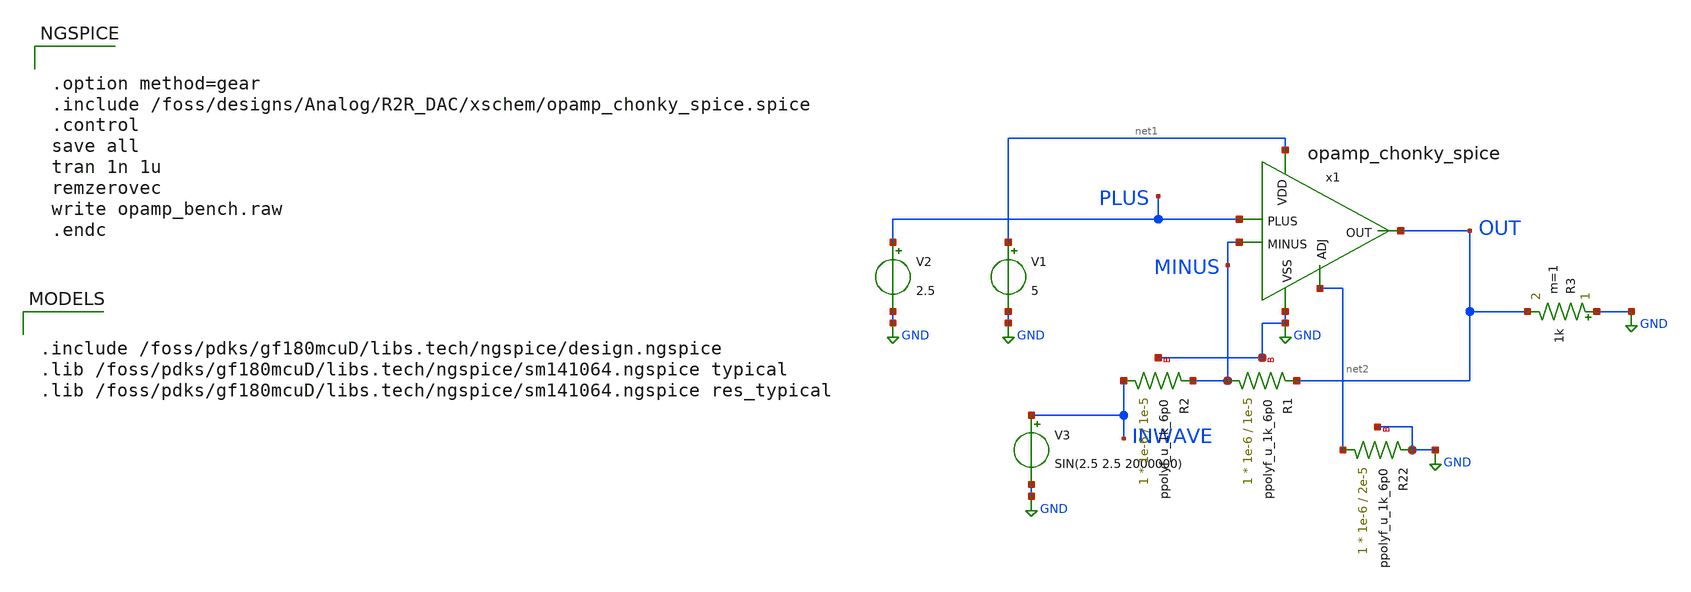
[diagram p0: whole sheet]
** sch_path: macros/Analog/R2R_DAC/xschem/opamp_bench.sch
**.subckt opamp_bench
V1 net1 GND 5
V2 PLUS GND 2.5
V3 INWAVE GND SIN(2.5 2.5 2000000)
XR22 net2 GND GND ppolyf_u_1k_6p0 r_width=1e-6 r_length=2e-5 m=1
R3 GND OUT 1k m=1
XR1 MINUS OUT GND ppolyf_u_1k_6p0 r_width=1e-6 r_length=1e-5 m=1
XR2 INWAVE MINUS GND ppolyf_u_1k_6p0 r_width=1e-6 r_length=1e-5 m=1
x1 PLUS MINUS net2 OUT net1 GND opamp_chonky_spice
**** begin user architecture code


.option method=gear
.include /foss/designs/Analog/R2R_DAC/xschem/opamp_chonky_spice.spice
.control
save all
tran 1n 1u
remzerovec
write opamp_bench.raw
.endc



.include /foss/pdks/gf180mcuD/libs.tech/ngspice/design.ngspice
.lib /foss/pdks/gf180mcuD/libs.tech/ngspice/sm141064.ngspice typical
.lib /foss/pdks/gf180mcuD/libs.tech/ngspice/sm141064.ngspice res_typical

**** end user architecture code
**.ends
.GLOBAL GND
.end
